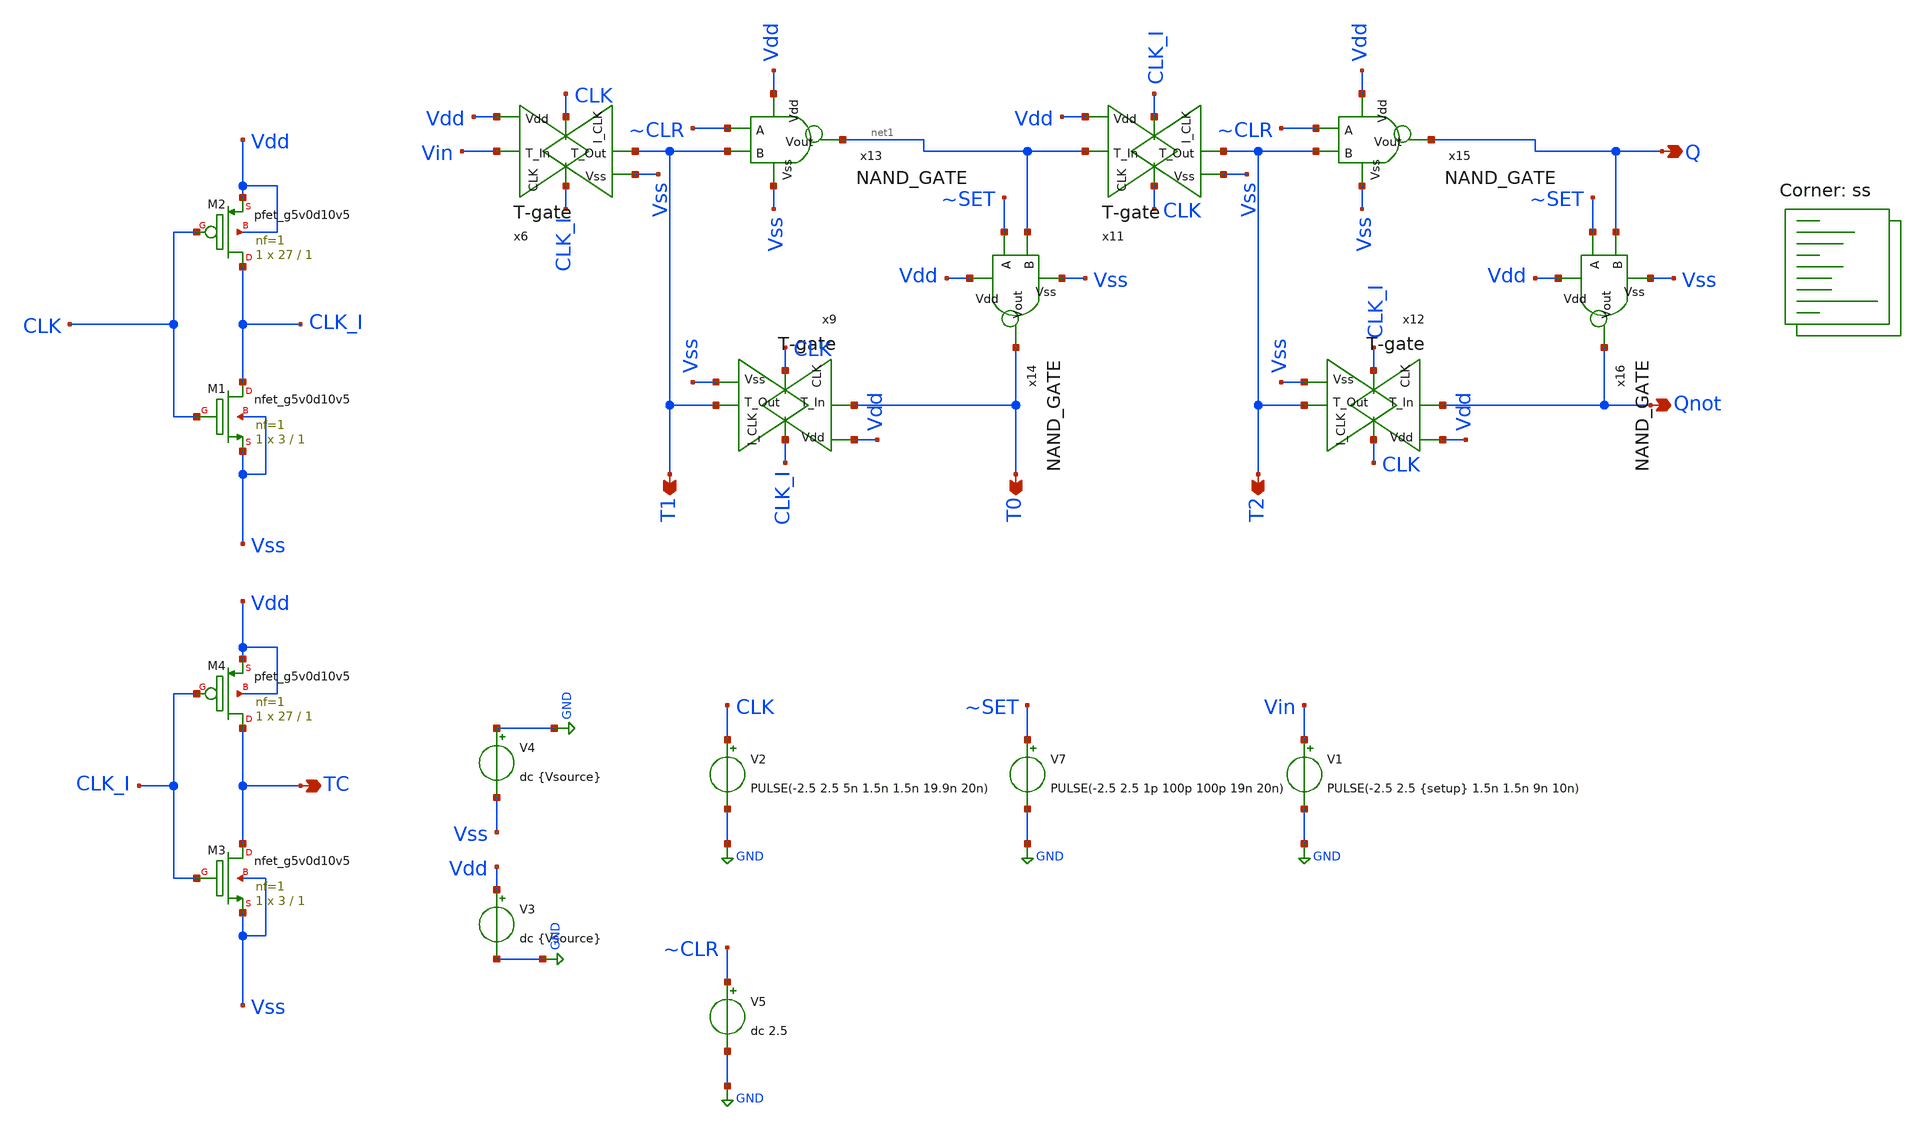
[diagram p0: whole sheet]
** sch_path: xschem/TGFF_TB.sch
**.subckt TGFF_TB Q Qnot T0 T1 T2 TC
*.opin Q
*.opin Qnot
*.opin T0
*.opin T1
*.opin T2
*.opin TC
V4 GND Vss dc {Vsource}
V3 Vdd GND dc {Vsource}
V1 Vin GND PULSE(-2.5 2.5 {setup} 1.5n 1.5n 9n 10n)
V2 CLK GND PULSE(-2.5 2.5 5n 1.5n 1.5n 19.9n 20n)
x6 CLK Vin T1 Vdd Vss CLK_I T-gate
x9 CLK_I T0 T1 Vdd Vss CLK T-gate
x11 CLK_I net1 T2 Vdd Vss CLK T-gate
x12 CLK Qnot T2 Vdd Vss CLK_I T-gate
x13 Vdd ~CLR T1 net1 Vss NAND_GATE
x14 Vdd ~SET net1 T0 Vss NAND_GATE
x15 Vdd ~CLR T2 Q Vss NAND_GATE
x16 Vdd ~SET Q Qnot Vss NAND_GATE
XM1 CLK_I CLK Vss Vss sky130_fd_pr__nfet_g5v0d10v5 L=1 W=3 nf=1 ad='int((1 + 1)/2) * 3 / 1 * 0.29' as='int((1 + 2)/2) * 3 / 1 * 0.29'
+ pd='2*int((1 + 1)/2) * (3 / 1 + 0.29)' ps='2*int((1 + 2)/2) * (3 / 1 + 0.29)' nrd='0.29 / 3 ' nrs='0.29 / 3 '
+ sa=0 sb=0 sd=0 mult=1 m=1
XM2 CLK_I CLK Vdd Vdd sky130_fd_pr__pfet_g5v0d10v5 L=1 W=27 nf=1 ad='int((1 + 1)/2) * 27 / 1 * 0.29'
+ as='int((1 + 2)/2) * 27 / 1 * 0.29' pd='2*int((1 + 1)/2) * (27 / 1 + 0.29)' ps='2*int((1 + 2)/2) * (27 / 1 + 0.29)'
+ nrd='0.29 / 27 ' nrs='0.29 / 27 ' sa=0 sb=0 sd=0 mult=1 m=1
XM3 TC CLK_I Vss Vss sky130_fd_pr__nfet_g5v0d10v5 L=1 W=3 nf=1 ad='int((1 + 1)/2) * 3 / 1 * 0.29' as='int((1 + 2)/2) * 3 / 1 * 0.29'
+ pd='2*int((1 + 1)/2) * (3 / 1 + 0.29)' ps='2*int((1 + 2)/2) * (3 / 1 + 0.29)' nrd='0.29 / 3 ' nrs='0.29 / 3 '
+ sa=0 sb=0 sd=0 mult=1 m=1
XM4 TC CLK_I Vdd Vdd sky130_fd_pr__pfet_g5v0d10v5 L=1 W=27 nf=1 ad='int((1 + 1)/2) * 27 / 1 * 0.29' as='int((1 + 2)/2) * 27 / 1 * 0.29'
+ pd='2*int((1 + 1)/2) * (27 / 1 + 0.29)' ps='2*int((1 + 2)/2) * (27 / 1 + 0.29)' nrd='0.29 / 27 ' nrs='0.29 / 27 '
+ sa=0 sb=0 sd=0 mult=1 m=1
V7 ~SET GND PULSE(-2.5 2.5 1p 100p 100p 19n 20n)
V5 ~CLR GND dc 2.5
**** begin user architecture code
.lib $::SKYWATER_MODELS/sky130.lib.spice ss



**** end user architecture code
**.ends

* expanding   symbol:  T-gate.sym # of pins=6
** sym_path: xschem/T-gate.sym
** sch_path: xschem/T-gate.sch
.subckt T-gate I_CLK T_In T_Out Vdd Vss CLK
*.ipin T_In
*.opin T_Out
*.ipin Vdd
*.ipin Vss
*.ipin I_CLK
*.ipin CLK
XM1 T_In I_CLK T_Out Vdd sky130_fd_pr__pfet_g5v0d10v5 L=0.5 W=3 nf=1 ad='int((1 + 1)/2) * 3 / 1 * 0.29'
+ as='int((1 + 2)/2) * 3 / 1 * 0.29' pd='2*int((1 + 1)/2) * (3 / 1 + 0.29)' ps='2*int((1 + 2)/2) * (3 / 1 + 0.29)'
+ nrd='0.29 / 3 ' nrs='0.29 / 3 ' sa=0 sb=0 sd=0 mult=1 m=1
XM3 T_Out CLK T_In Vss sky130_fd_pr__nfet_g5v0d10v5 L=0.5 W=1 nf=1 ad='int((1 + 1)/2) * 1 / 1 * 0.29'
+ as='int((1 + 2)/2) * 1 / 1 * 0.29' pd='2*int((1 + 1)/2) * (1 / 1 + 0.29)' ps='2*int((1 + 2)/2) * (1 / 1 + 0.29)'
+ nrd='0.29 / 1 ' nrs='0.29 / 1 ' sa=0 sb=0 sd=0 mult=1 m=1
XM2 T_Out CLK T_Out Vdd sky130_fd_pr__pfet_g5v0d10v5 L=0.5 W=1.5 nf=1 ad='int((1 + 1)/2) * 1.5 / 1 * 0.29'
+ as='int((1 + 2)/2) * 1.5 / 1 * 0.29' pd='2*int((1 + 1)/2) * (1.5 / 1 + 0.29)' ps='2*int((1 + 2)/2) * (1.5 / 1 + 0.29)'
+ nrd='0.29 / 1.5 ' nrs='0.29 / 1.5 ' sa=0 sb=0 sd=0 mult=1 m=1
XM4 T_In CLK T_In Vdd sky130_fd_pr__pfet_g5v0d10v5 L=0.5 W=1.5 nf=1 ad='int((1 + 1)/2) * 1.5 / 1 * 0.29'
+ as='int((1 + 2)/2) * 1.5 / 1 * 0.29' pd='2*int((1 + 1)/2) * (1.5 / 1 + 0.29)' ps='2*int((1 + 2)/2) * (1.5 / 1 + 0.29)'
+ nrd='0.29 / 1.5 ' nrs='0.29 / 1.5 ' sa=0 sb=0 sd=0 mult=1 m=1
XM5 T_In I_CLK T_In Vss sky130_fd_pr__nfet_g5v0d10v5 L=0.5 W=0.5 nf=1 ad='int((1 + 1)/2) * 0.5 / 1 * 0.29'
+ as='int((1 + 2)/2) * 0.5 / 1 * 0.29' pd='2*int((1 + 1)/2) * (0.5 / 1 + 0.29)' ps='2*int((1 + 2)/2) * (0.5 / 1 + 0.29)'
+ nrd='0.29 / 0.5 ' nrs='0.29 / 0.5 ' sa=0 sb=0 sd=0 mult=1 m=1
XM6 T_Out I_CLK T_Out Vss sky130_fd_pr__nfet_g5v0d10v5 L=0.5 W=0.5 nf=1 ad='int((1 + 1)/2) * 0.5 / 1 * 0.29'
+ as='int((1 + 2)/2) * 0.5 / 1 * 0.29' pd='2*int((1 + 1)/2) * (0.5 / 1 + 0.29)' ps='2*int((1 + 2)/2) * (0.5 / 1 + 0.29)'
+ nrd='0.29 / 0.5 ' nrs='0.29 / 0.5 ' sa=0 sb=0 sd=0 mult=1 m=1
.ends


* expanding   symbol:  NAND_GATE.sym # of pins=5
** sym_path: xschem/NAND_GATE.sym
** sch_path: xschem/NAND_GATE.sch
.subckt NAND_GATE Vdd A B Vout Vss
*.ipin Vdd
*.ipin Vss
*.ipin A
*.ipin B
*.opin Vout
XM3 Vout A net1 Vss sky130_fd_pr__nfet_g5v0d10v5 L=0.5 W=1 nf=1 ad='int((1 + 1)/2) * 1 / 1 * 0.29' as='int((1 + 2)/2) * 1 / 1 * 0.29'
+ pd='2*int((1 + 1)/2) * (1 / 1 + 0.29)' ps='2*int((1 + 2)/2) * (1 / 1 + 0.29)' nrd='0.29 / 1 ' nrs='0.29 / 1 '
+ sa=0 sb=0 sd=0 mult=1 m=1
XM4 Vout A Vdd Vdd sky130_fd_pr__pfet_g5v0d10v5 L=0.5 W=3 nf=1 ad='int((1 + 1)/2) * 3 / 1 * 0.29' as='int((1 + 2)/2) * 3 / 1 * 0.29'
+ pd='2*int((1 + 1)/2) * (3 / 1 + 0.29)' ps='2*int((1 + 2)/2) * (3 / 1 + 0.29)' nrd='0.29 / 3 ' nrs='0.29 / 3 '
+ sa=0 sb=0 sd=0 mult=1 m=1
XM5 Vout B Vdd Vdd sky130_fd_pr__pfet_g5v0d10v5 L=0.5 W=3 nf=1 ad='int((1 + 1)/2) * 3 / 1 * 0.29' as='int((1 + 2)/2) * 3 / 1 * 0.29'
+ pd='2*int((1 + 1)/2) * (3 / 1 + 0.29)' ps='2*int((1 + 2)/2) * (3 / 1 + 0.29)' nrd='0.29 / 3 ' nrs='0.29 / 3 '
+ sa=0 sb=0 sd=0 mult=1 m=1
XM1 net1 B Vss Vss sky130_fd_pr__nfet_g5v0d10v5 L=0.5 W=1 nf=1 ad='int((1 + 1)/2) * 1 / 1 * 0.29' as='int((1 + 2)/2) * 1 / 1 * 0.29'
+ pd='2*int((1 + 1)/2) * (1 / 1 + 0.29)' ps='2*int((1 + 2)/2) * (1 / 1 + 0.29)' nrd='0.29 / 1 ' nrs='0.29 / 1 '
+ sa=0 sb=0 sd=0 mult=1 m=1
.ends

.GLOBAL GND
.end
